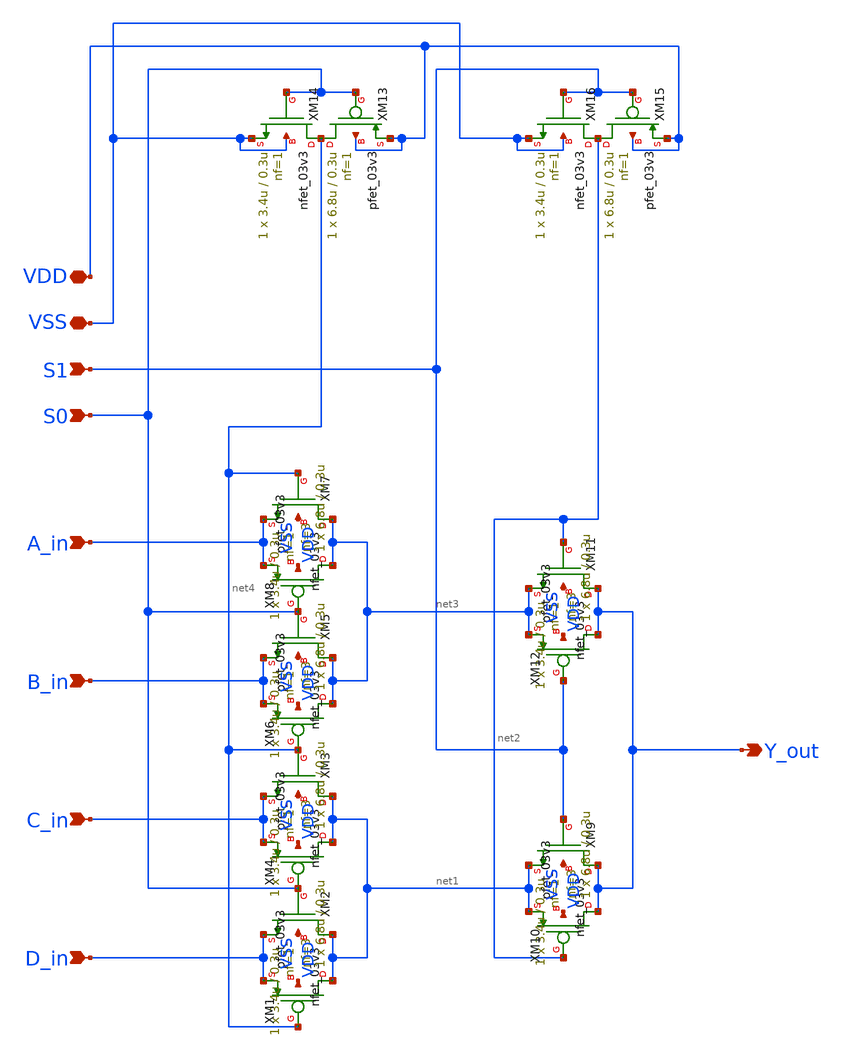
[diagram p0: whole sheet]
** sch_path: MUX41/PTL/Mux41PTL/Mux41PTL.sch
**.subckt Mux41PTL D_in C_in B_in A_in S0 S1 VSS VDD Y_out
*.ipin D_in
*.ipin C_in
*.ipin B_in
*.ipin A_in
*.ipin S0
*.ipin S1
*.iopin VSS
*.iopin VDD
*.opin Y_out
XM2 net1 S0 D_in VSS nfet_03v3 L=0.3u W=3.4u nf=1 ad='int((nf+1)/2) * W/nf * 0.18u' as='int((nf+2)/2) * W/nf * 0.18u'
+ pd='2*int((nf+1)/2) * (W/nf + 0.18u)' ps='2*int((nf+2)/2) * (W/nf + 0.18u)' nrd='0.18u / W' nrs='0.18u / W'
+ sa=0 sb=0 sd=0 m=1
XM14 net4 S0 VSS VSS nfet_03v3 L=0.3u W=3.4u nf=1 ad='int((nf+1)/2) * W/nf * 0.18u' as='int((nf+2)/2) * W/nf * 0.18u'
+ pd='2*int((nf+1)/2) * (W/nf + 0.18u)' ps='2*int((nf+2)/2) * (W/nf + 0.18u)' nrd='0.18u / W' nrs='0.18u / W'
+ sa=0 sb=0 sd=0 m=1
XM13 net4 S0 VDD VDD pfet_03v3 L=0.3u W=6.8u nf=1 ad='int((nf+1)/2) * W/nf * 0.18u' as='int((nf+2)/2) * W/nf * 0.18u'
+ pd='2*int((nf+1)/2) * (W/nf + 0.18u)' ps='2*int((nf+2)/2) * (W/nf + 0.18u)' nrd='0.18u / W' nrs='0.18u / W'
+ sa=0 sb=0 sd=0 m=1
XM16 net2 S1 VSS VSS nfet_03v3 L=0.3u W=3.4u nf=1 ad='int((nf+1)/2) * W/nf * 0.18u' as='int((nf+2)/2) * W/nf * 0.18u'
+ pd='2*int((nf+1)/2) * (W/nf + 0.18u)' ps='2*int((nf+2)/2) * (W/nf + 0.18u)' nrd='0.18u / W' nrs='0.18u / W'
+ sa=0 sb=0 sd=0 m=1
XM15 net2 S1 VDD VDD pfet_03v3 L=0.3u W=6.8u nf=1 ad='int((nf+1)/2) * W/nf * 0.18u' as='int((nf+2)/2) * W/nf * 0.18u'
+ pd='2*int((nf+1)/2) * (W/nf + 0.18u)' ps='2*int((nf+2)/2) * (W/nf + 0.18u)' nrd='0.18u / W' nrs='0.18u / W'
+ sa=0 sb=0 sd=0 m=1
XM1 net1 net4 D_in VDD pfet_03v3 L=0.3u W=6.8u nf=3 ad='int((nf+1)/2) * W/nf * 0.18u' as='int((nf+2)/2) * W/nf * 0.18u'
+ pd='2*int((nf+1)/2) * (W/nf + 0.18u)' ps='2*int((nf+2)/2) * (W/nf + 0.18u)' nrd='0.18u / W' nrs='0.18u / W'
+ sa=0 sb=0 sd=0 m=1
XM3 net1 net4 C_in VSS nfet_03v3 L=0.3u W=3.4u nf=1 ad='int((nf+1)/2) * W/nf * 0.18u' as='int((nf+2)/2) * W/nf * 0.18u'
+ pd='2*int((nf+1)/2) * (W/nf + 0.18u)' ps='2*int((nf+2)/2) * (W/nf + 0.18u)' nrd='0.18u / W' nrs='0.18u / W'
+ sa=0 sb=0 sd=0 m=1
XM4 net1 S0 C_in VDD pfet_03v3 L=0.3u W=6.8u nf=3 ad='int((nf+1)/2) * W/nf * 0.18u' as='int((nf+2)/2) * W/nf * 0.18u'
+ pd='2*int((nf+1)/2) * (W/nf + 0.18u)' ps='2*int((nf+2)/2) * (W/nf + 0.18u)' nrd='0.18u / W' nrs='0.18u / W'
+ sa=0 sb=0 sd=0 m=1
XM5 net3 S0 B_in VSS nfet_03v3 L=0.3u W=3.4u nf=1 ad='int((nf+1)/2) * W/nf * 0.18u' as='int((nf+2)/2) * W/nf * 0.18u'
+ pd='2*int((nf+1)/2) * (W/nf + 0.18u)' ps='2*int((nf+2)/2) * (W/nf + 0.18u)' nrd='0.18u / W' nrs='0.18u / W'
+ sa=0 sb=0 sd=0 m=1
XM6 net3 net4 B_in VDD pfet_03v3 L=0.3u W=6.8u nf=3 ad='int((nf+1)/2) * W/nf * 0.18u' as='int((nf+2)/2) * W/nf * 0.18u'
+ pd='2*int((nf+1)/2) * (W/nf + 0.18u)' ps='2*int((nf+2)/2) * (W/nf + 0.18u)' nrd='0.18u / W' nrs='0.18u / W'
+ sa=0 sb=0 sd=0 m=1
XM7 net3 net4 A_in VSS nfet_03v3 L=0.3u W=3.4u nf=1 ad='int((nf+1)/2) * W/nf * 0.18u' as='int((nf+2)/2) * W/nf * 0.18u'
+ pd='2*int((nf+1)/2) * (W/nf + 0.18u)' ps='2*int((nf+2)/2) * (W/nf + 0.18u)' nrd='0.18u / W' nrs='0.18u / W'
+ sa=0 sb=0 sd=0 m=1
XM8 net3 S0 A_in VDD pfet_03v3 L=0.3u W=6.8u nf=3 ad='int((nf+1)/2) * W/nf * 0.18u' as='int((nf+2)/2) * W/nf * 0.18u'
+ pd='2*int((nf+1)/2) * (W/nf + 0.18u)' ps='2*int((nf+2)/2) * (W/nf + 0.18u)' nrd='0.18u / W' nrs='0.18u / W'
+ sa=0 sb=0 sd=0 m=1
XM9 Y_out S1 net1 VSS nfet_03v3 L=0.3u W=3.4u nf=1 ad='int((nf+1)/2) * W/nf * 0.18u' as='int((nf+2)/2) * W/nf * 0.18u'
+ pd='2*int((nf+1)/2) * (W/nf + 0.18u)' ps='2*int((nf+2)/2) * (W/nf + 0.18u)' nrd='0.18u / W' nrs='0.18u / W'
+ sa=0 sb=0 sd=0 m=1
XM10 Y_out net2 net1 VDD pfet_03v3 L=0.3u W=6.8u nf=3 ad='int((nf+1)/2) * W/nf * 0.18u' as='int((nf+2)/2) * W/nf * 0.18u'
+ pd='2*int((nf+1)/2) * (W/nf + 0.18u)' ps='2*int((nf+2)/2) * (W/nf + 0.18u)' nrd='0.18u / W' nrs='0.18u / W'
+ sa=0 sb=0 sd=0 m=1
XM11 Y_out net2 net3 VSS nfet_03v3 L=0.3u W=3.4u nf=1 ad='int((nf+1)/2) * W/nf * 0.18u' as='int((nf+2)/2) * W/nf * 0.18u'
+ pd='2*int((nf+1)/2) * (W/nf + 0.18u)' ps='2*int((nf+2)/2) * (W/nf + 0.18u)' nrd='0.18u / W' nrs='0.18u / W'
+ sa=0 sb=0 sd=0 m=1
XM12 Y_out S1 net3 VDD pfet_03v3 L=0.3u W=6.8u nf=3 ad='int((nf+1)/2) * W/nf * 0.18u' as='int((nf+2)/2) * W/nf * 0.18u'
+ pd='2*int((nf+1)/2) * (W/nf + 0.18u)' ps='2*int((nf+2)/2) * (W/nf + 0.18u)' nrd='0.18u / W' nrs='0.18u / W'
+ sa=0 sb=0 sd=0 m=1
**.ends
.end
